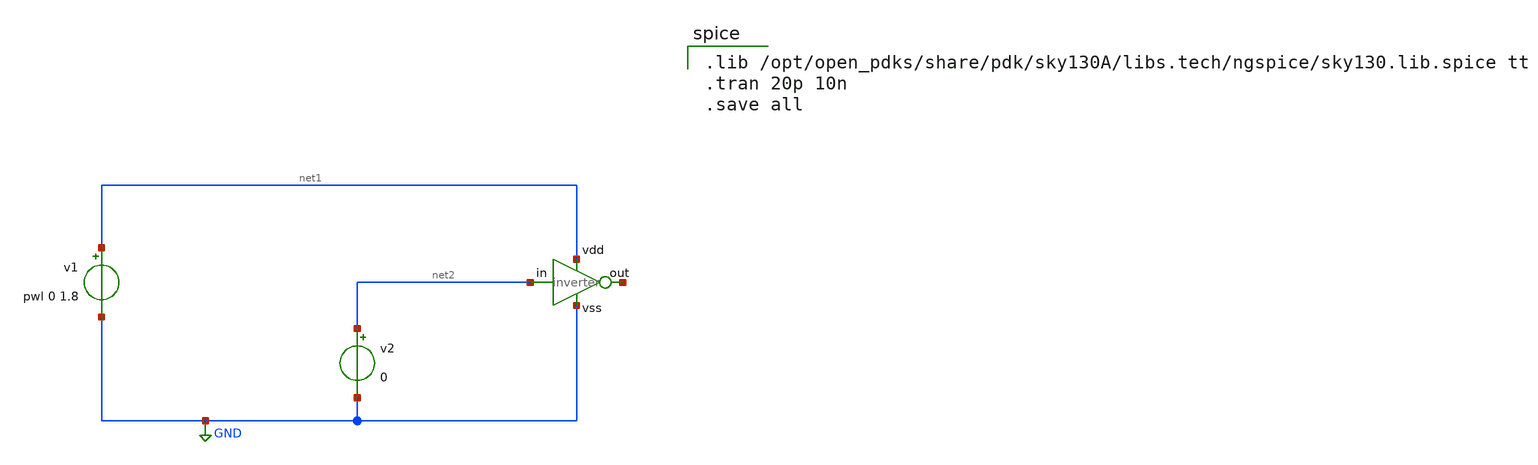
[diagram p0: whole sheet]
** sch_path: projects/carry_lookahead_adder/xschem/ports/test/true_table/inverter.sch
**.subckt inverter
v1 net1 GND pwl 0 1.8
v2 net2 GND 0
x1 net2 net3 net1 GND inverter
**** begin user architecture code

.lib /opt/open_pdks/share/pdk/sky130A/libs.tech/ngspice/sky130.lib.spice tt
.tran 20p 10n
.save all

**** end user architecture code
**.ends

* expanding   symbol:
*+  /home/peppe/Desktop/vlsi/circuits-simulation/projects/carry_lookahead_adder/xschem/ports/inverter.sym # of pins=4
** sym_path: projects/carry_lookahead_adder/xschem/ports/inverter.sym
** sch_path: projects/carry_lookahead_adder/xschem/ports/inverter.sch
.subckt inverter in out vdd vss
*.ipin in
*.ipin vdd
*.ipin vss
*.opin out
XM2 out in vss vss sky130_fd_pr__nfet_01v8 L=0.15 W=1 nf=1 ad='W * 0.29' as='W * 0.29' pd='W + 2 * 0.29'
+ ps='W + 2 * 0.29' nrd=0 nrs=0 sa=0 sb=0 sd=0 mult=1 m=1
XM1 out in vdd vdd sky130_fd_pr__pfet_01v8 L=0.15 W=3 nf=1 ad='W * 0.29' as='W * 0.29' pd='W + 2 * 0.29'
+ ps='W + 2 * 0.29' nrd=0 nrs=0 sa=0 sb=0 sd=0 mult=1 m=1
.ends

.GLOBAL GND
.end
